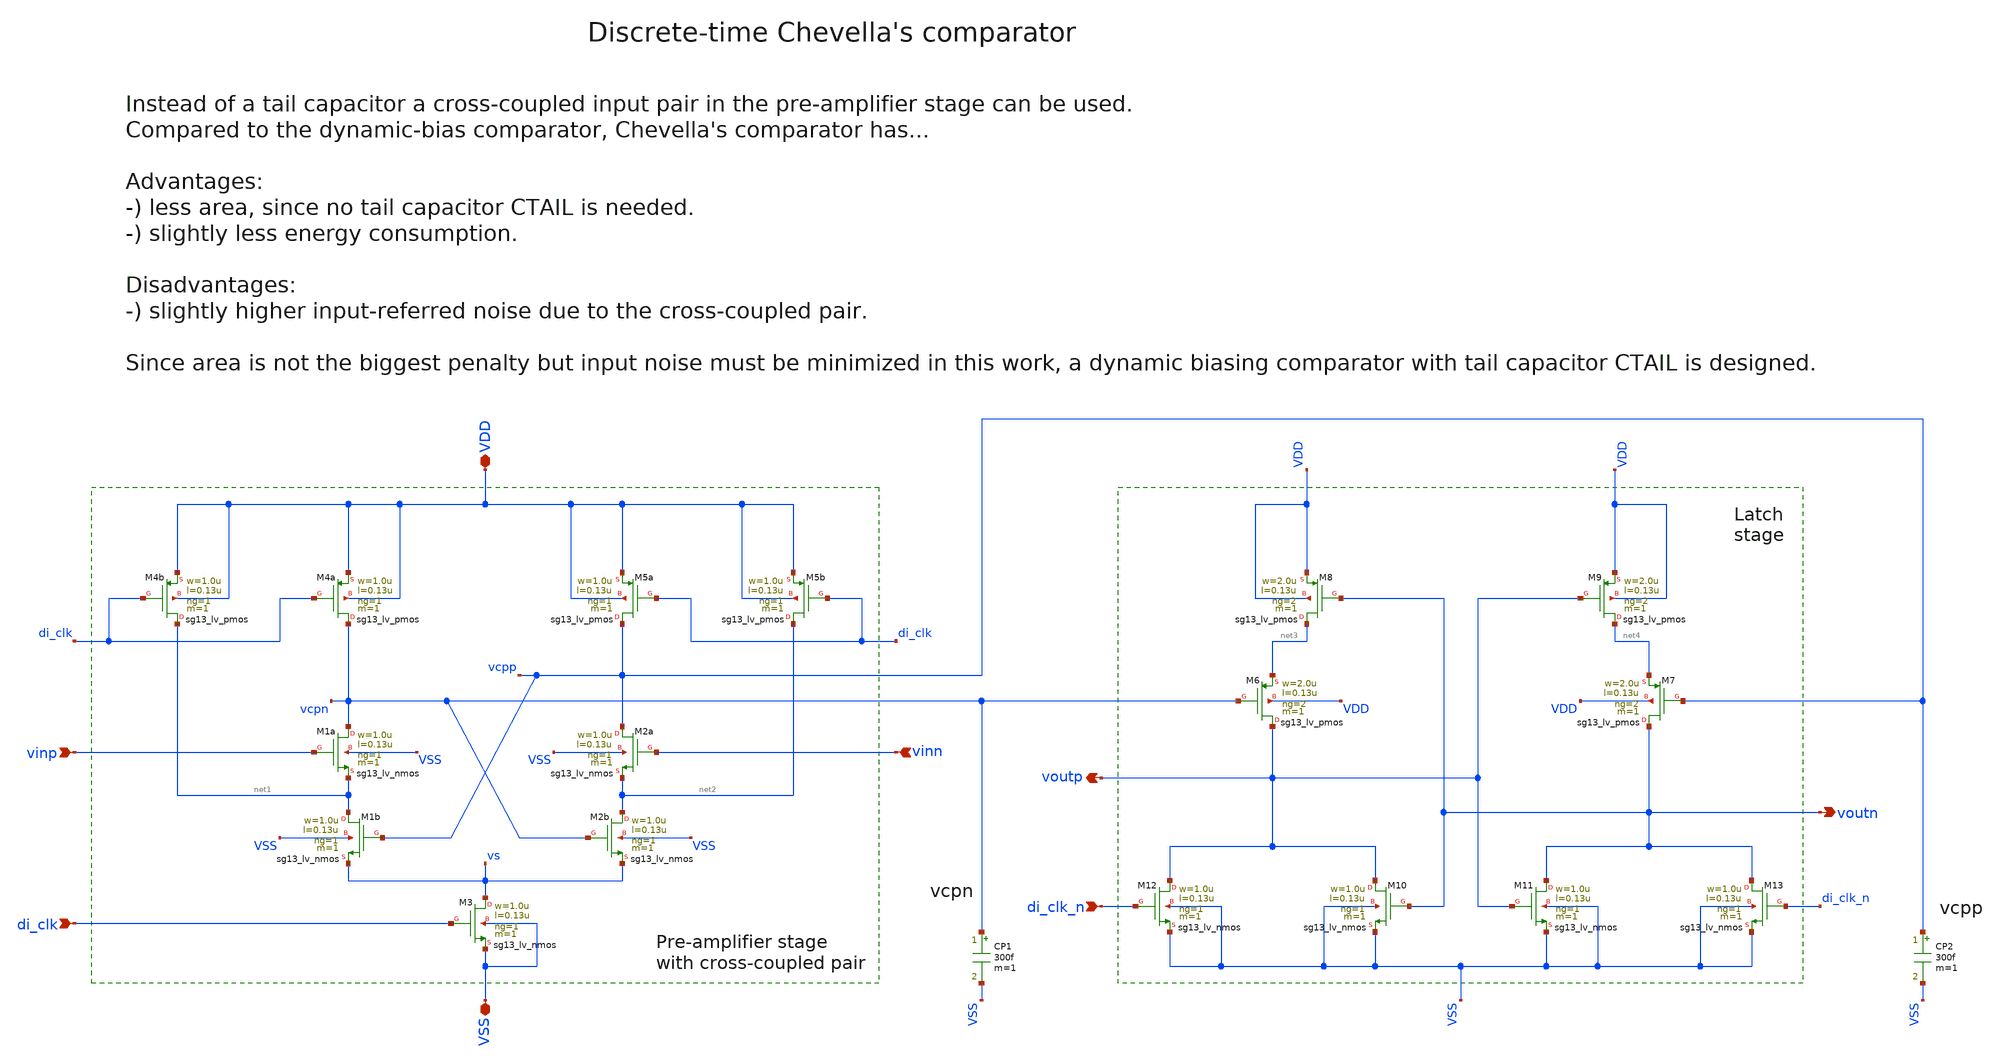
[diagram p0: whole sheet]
** sch_path: SG13G2_ATBS-ADC-main/xschem/comparator/discrete_time/Chevella/Chevella_comparator.sch
**.subckt Chevella_comparator VDD voutp voutn di_clk_n VSS vinp vinn di_clk
*.iopin VDD
*.opin voutp
*.opin voutn
*.ipin di_clk_n
*.iopin VSS
*.ipin vinp
*.ipin vinn
*.ipin di_clk
XM1a vcpn vinp net1 VSS sg13_lv_nmos w=1.0u l=0.13u ng=1 m=1 mm_ok=1
XM2a vcpp vinn net2 VSS sg13_lv_nmos w=1.0u l=0.13u ng=1 m=1 mm_ok=1
XM3 vs di_clk VSS VSS sg13_lv_nmos w=1.0u l=0.13u ng=1 m=1 mm_ok=1
XM4a vcpn di_clk VDD VDD sg13_lv_pmos w=1.0u l=0.13u ng=1 m=1 mm_ok=1
XM5a vcpp di_clk VDD VDD sg13_lv_pmos w=1.0u l=0.13u ng=1 m=1 mm_ok=1
XM12 voutp di_clk_n VSS VSS sg13_lv_nmos w=1.0u l=0.13u ng=1 m=1 mm_ok=1
XM8 net3 voutn VDD VDD sg13_lv_pmos w=2.0u l=0.13u ng=2 m=1 mm_ok=1
XM10 voutp voutn VSS VSS sg13_lv_nmos w=1.0u l=0.13u ng=1 m=1 mm_ok=1
XM11 voutn voutp VSS VSS sg13_lv_nmos w=1.0u l=0.13u ng=1 m=1 mm_ok=1
XM13 voutn di_clk_n VSS VSS sg13_lv_nmos w=1.0u l=0.13u ng=1 m=1 mm_ok=1
CP1 vcpn VSS 300f m=1
CP2 vcpp VSS 300f m=1
XM9 net4 voutp VDD VDD sg13_lv_pmos w=2.0u l=0.13u ng=2 m=1 mm_ok=1
XM6 voutp vcpn net3 VDD sg13_lv_pmos w=2.0u l=0.13u ng=2 m=1 mm_ok=1
XM7 voutn vcpp net4 VDD sg13_lv_pmos w=2.0u l=0.13u ng=2 m=1 mm_ok=1
XM4b net1 di_clk VDD VDD sg13_lv_pmos w=1.0u l=0.13u ng=1 m=1 mm_ok=1
XM5b net2 di_clk VDD VDD sg13_lv_pmos w=1.0u l=0.13u ng=1 m=1 mm_ok=1
XM1b net1 vcpp vs VSS sg13_lv_nmos w=1.0u l=0.13u ng=1 m=1 mm_ok=1
XM2b net2 vcpn vs VSS sg13_lv_nmos w=1.0u l=0.13u ng=1 m=1 mm_ok=1
**.ends
.end
